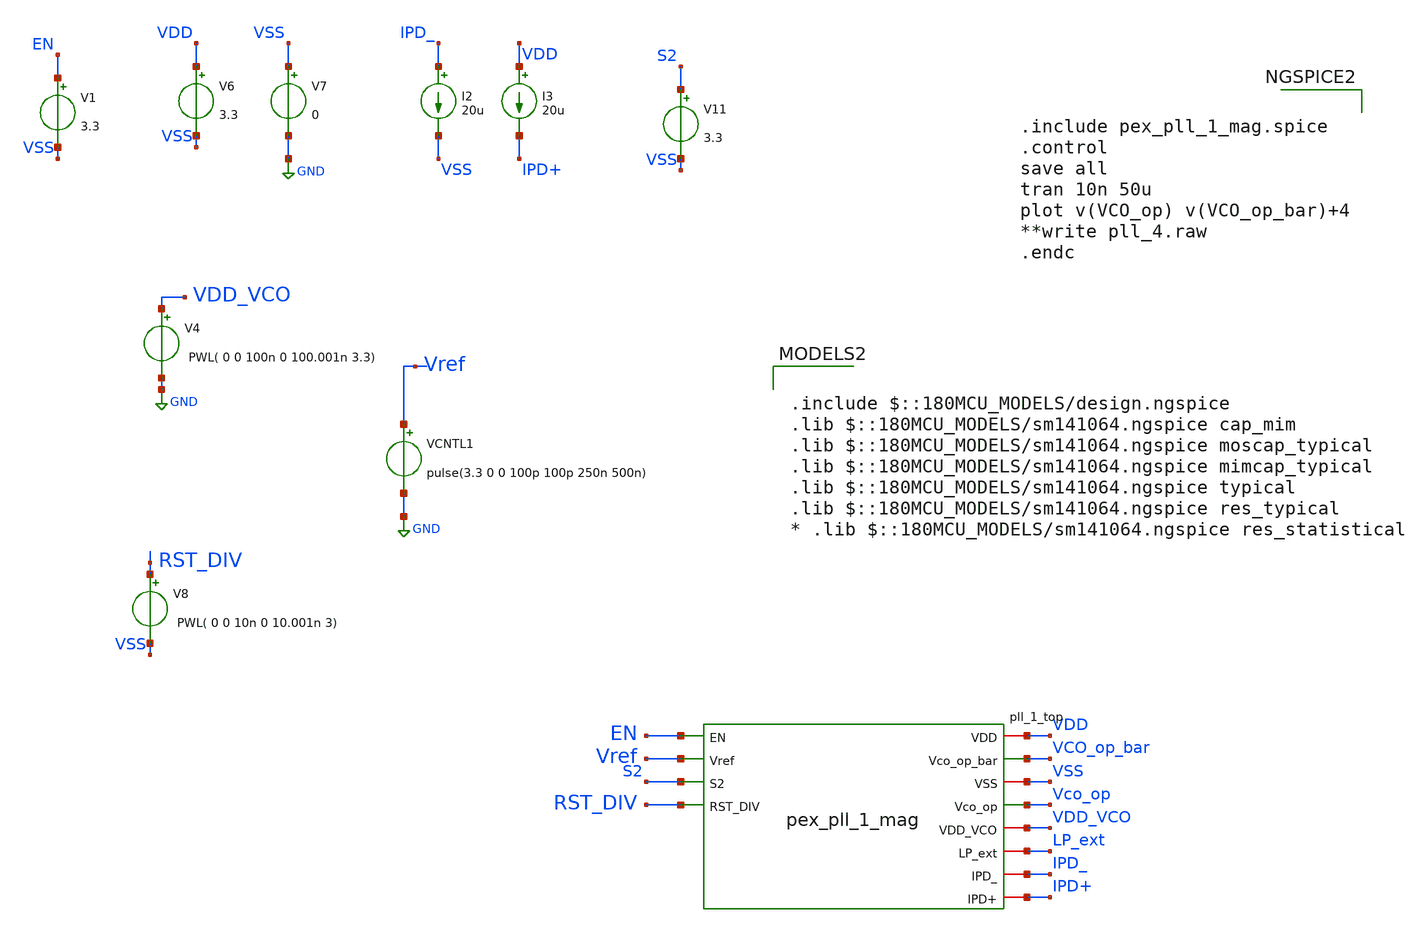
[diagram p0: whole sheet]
** sch_path: Clock_Generator_PAKISTAN_02/Schematics/pex_pll_1_top_TB.sch
**.subckt pex_pll_1_top_TB
VCNTL1 Vref GND pulse(3.3 0 0 100p 100p 250n 500n)
V4 VDD_VCO GND PWL( 0 0 100n 0 100.001n 3.3)
V6 VDD VSS 3.3
V7 VSS GND 0
V8 RST_DIV VSS PWL( 0 0 10n 0 10.001n 3)
V11 S2 VSS 3.3
I2 IPD_ VSS 20u
I3 VDD IPD+ 20u
V1 EN VSS 3.3
x1 VDD EN VCO_op_bar Vref VSS Vco_op S2 VDD_VCO RST_DIV LP_ext IPD_ IPD+ pex_pll_1_mag
**** begin user architecture code


.include pex_pll_1_mag.spice
.control
save all
tran 10n 50u
plot v(VCO_op) v(VCO_op_bar)+4
**write pll_4.raw
.endc



.include $::180MCU_MODELS/design.ngspice
.lib $::180MCU_MODELS/sm141064.ngspice cap_mim
.lib $::180MCU_MODELS/sm141064.ngspice moscap_typical
.lib $::180MCU_MODELS/sm141064.ngspice mimcap_typical
.lib $::180MCU_MODELS/sm141064.ngspice typical
.lib $::180MCU_MODELS/sm141064.ngspice res_typical
* .lib $::180MCU_MODELS/sm141064.ngspice res_statistical

**** end user architecture code
**.ends
.GLOBAL GND
.end
